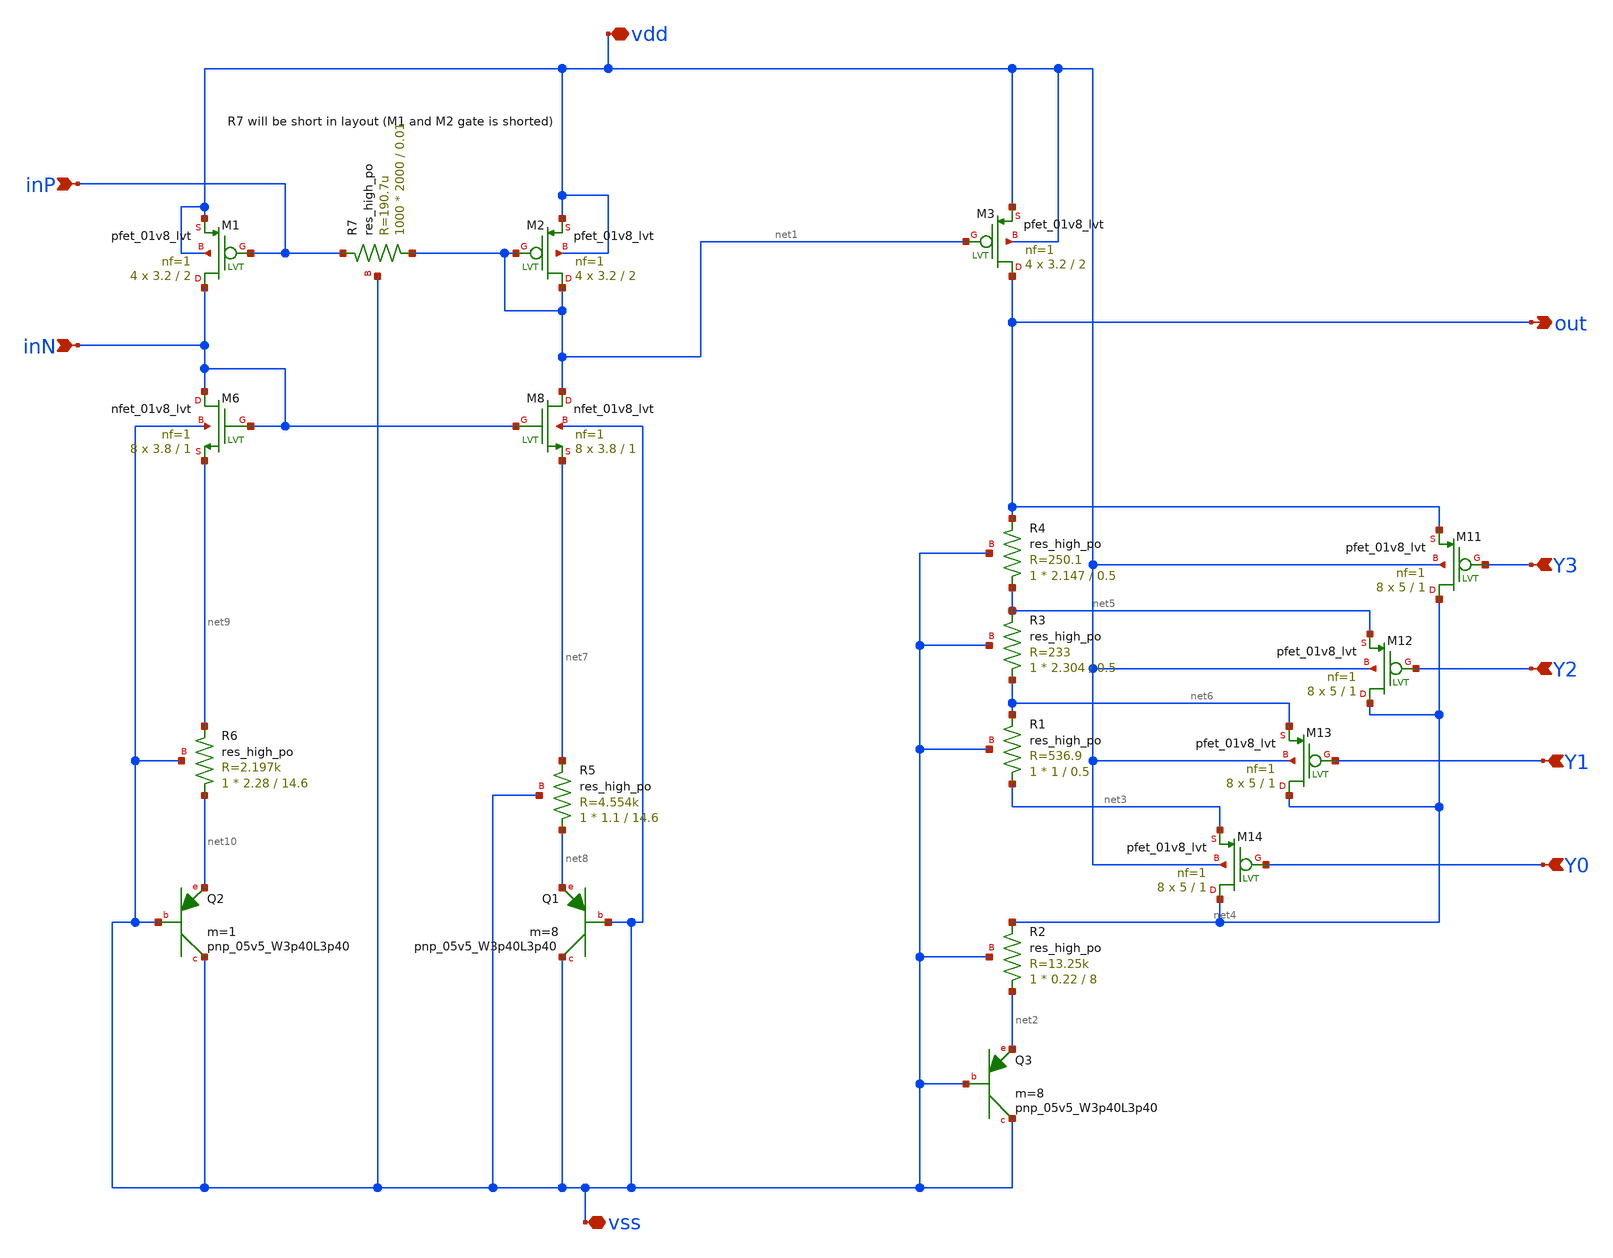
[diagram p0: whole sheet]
** sch_path: BGR_coreAndVrefBranch.sch
**.subckt BGR_coreAndVrefBranch out vss Y3 Y2 Y1 Y0 vdd inP inN
*.opin out
*.iopin vss
*.ipin Y3
*.ipin Y2
*.ipin Y1
*.ipin Y0
*.iopin vdd
*.ipin inP
*.ipin inN
XM3 out net1 vdd vdd sky130_fd_pr__pfet_01v8_lvt L=2 W=3.2 nf=1 ad='int((1 + 1)/2) * 3.2 / 1 * 0.29'
+ as='int((1 + 2)/2) * 3.2 / 1 * 0.29' pd='2*int((1 + 1)/2) * (3.2 / 1 + 0.29)' ps='2*int((1 + 2)/2) * (3.2 / 1 + 0.29)'
+ nrd='0.29 / 3.2 ' nrs='0.29 / 3.2 ' sa=0 sb=0 sd=0 mult=4 m=4
XQ3 vss vss net2 sky130_fd_pr__pnp_05v5_W3p40L3p40 m=8
XR2 net2 net4 vss sky130_fd_pr__res_high_po W=0.22 L=8 mult=1 m=1
XM11 net4 Y3 out vdd sky130_fd_pr__pfet_01v8_lvt L=1 W=5 nf=1 ad='int((1 + 1)/2) * 5 / 1 * 0.29' as='int((1 + 2)/2) * 5 / 1 * 0.29'
+ pd='2*int((1 + 1)/2) * (5 / 1 + 0.29)' ps='2*int((1 + 2)/2) * (5 / 1 + 0.29)' nrd='0.29 / 5 ' nrs='0.29 / 5 '
+ sa=0 sb=0 sd=0 mult=8 m=8
XM12 net4 Y2 net5 vdd sky130_fd_pr__pfet_01v8_lvt L=1 W=5 nf=1 ad='int((1 + 1)/2) * 5 / 1 * 0.29' as='int((1 + 2)/2) * 5 / 1 * 0.29'
+ pd='2*int((1 + 1)/2) * (5 / 1 + 0.29)' ps='2*int((1 + 2)/2) * (5 / 1 + 0.29)' nrd='0.29 / 5 ' nrs='0.29 / 5 '
+ sa=0 sb=0 sd=0 mult=8 m=8
XM13 net4 Y1 net6 vdd sky130_fd_pr__pfet_01v8_lvt L=1 W=5 nf=1 ad='int((1 + 1)/2) * 5 / 1 * 0.29' as='int((1 + 2)/2) * 5 / 1 * 0.29'
+ pd='2*int((1 + 1)/2) * (5 / 1 + 0.29)' ps='2*int((1 + 2)/2) * (5 / 1 + 0.29)' nrd='0.29 / 5 ' nrs='0.29 / 5 '
+ sa=0 sb=0 sd=0 mult=8 m=8
XM14 net4 Y0 net3 vdd sky130_fd_pr__pfet_01v8_lvt L=1 W=5 nf=1 ad='int((1 + 1)/2) * 5 / 1 * 0.29' as='int((1 + 2)/2) * 5 / 1 * 0.29'
+ pd='2*int((1 + 1)/2) * (5 / 1 + 0.29)' ps='2*int((1 + 2)/2) * (5 / 1 + 0.29)' nrd='0.29 / 5 ' nrs='0.29 / 5 '
+ sa=0 sb=0 sd=0 mult=8 m=8
XR1 net3 net6 vss sky130_fd_pr__res_high_po W=1 L=0.5 mult=1 m=1
XR3 net6 net5 vss sky130_fd_pr__res_high_po W=2.304 L=0.5 mult=1 m=1
XR4 net5 out vss sky130_fd_pr__res_high_po W=2.147 L=0.5 mult=1 m=1
XM6 inN inN net9 vss sky130_fd_pr__nfet_01v8_lvt L=1 W=3.8 nf=1 ad='int((1 + 1)/2) * 3.8 / 1 * 0.29'
+ as='int((1 + 2)/2) * 3.8 / 1 * 0.29' pd='2*int((1 + 1)/2) * (3.8 / 1 + 0.29)' ps='2*int((1 + 2)/2) * (3.8 / 1 + 0.29)'
+ nrd='0.29 / 3.8 ' nrs='0.29 / 3.8 ' sa=0 sb=0 sd=0 mult=8 m=8
XM1 inN inP vdd vdd sky130_fd_pr__pfet_01v8_lvt L=2 W=3.2 nf=1 ad='int((1 + 1)/2) * 3.2 / 1 * 0.29' as='int((1 + 2)/2) * 3.2 / 1 * 0.29'
+ pd='2*int((1 + 1)/2) * (3.2 / 1 + 0.29)' ps='2*int((1 + 2)/2) * (3.2 / 1 + 0.29)' nrd='0.29 / 3.2 ' nrs='0.29 / 3.2 '
+ sa=0 sb=0 sd=0 mult=4 m=4
XQ1 vss vss net8 sky130_fd_pr__pnp_05v5_W3p40L3p40 m=8
XR5 net8 net7 vss sky130_fd_pr__res_high_po W=1.1 L=14.6 mult=1 m=1
XM2 net1 net1 vdd vdd sky130_fd_pr__pfet_01v8_lvt L=2 W=3.2 nf=1 ad='int((1 + 1)/2) * 3.2 / 1 * 0.29'
+ as='int((1 + 2)/2) * 3.2 / 1 * 0.29' pd='2*int((1 + 1)/2) * (3.2 / 1 + 0.29)' ps='2*int((1 + 2)/2) * (3.2 / 1 + 0.29)'
+ nrd='0.29 / 3.2 ' nrs='0.29 / 3.2 ' sa=0 sb=0 sd=0 mult=4 m=4
XM8 net1 inN net7 vss sky130_fd_pr__nfet_01v8_lvt L=1 W=3.8 nf=1 ad='int((1 + 1)/2) * 3.8 / 1 * 0.29'
+ as='int((1 + 2)/2) * 3.8 / 1 * 0.29' pd='2*int((1 + 1)/2) * (3.8 / 1 + 0.29)' ps='2*int((1 + 2)/2) * (3.8 / 1 + 0.29)'
+ nrd='0.29 / 3.8 ' nrs='0.29 / 3.8 ' sa=0 sb=0 sd=0 mult=8 m=8
XQ2 vss vss net10 sky130_fd_pr__pnp_05v5_W3p40L3p40 m=1
XR6 net10 net9 vss sky130_fd_pr__res_high_po W=2.28 L=14.6 mult=1 m=1
XR7 net1 inP vss sky130_fd_pr__res_high_po W=2000 L=0.01 mult=1000 m=1000
**.ends
.end
